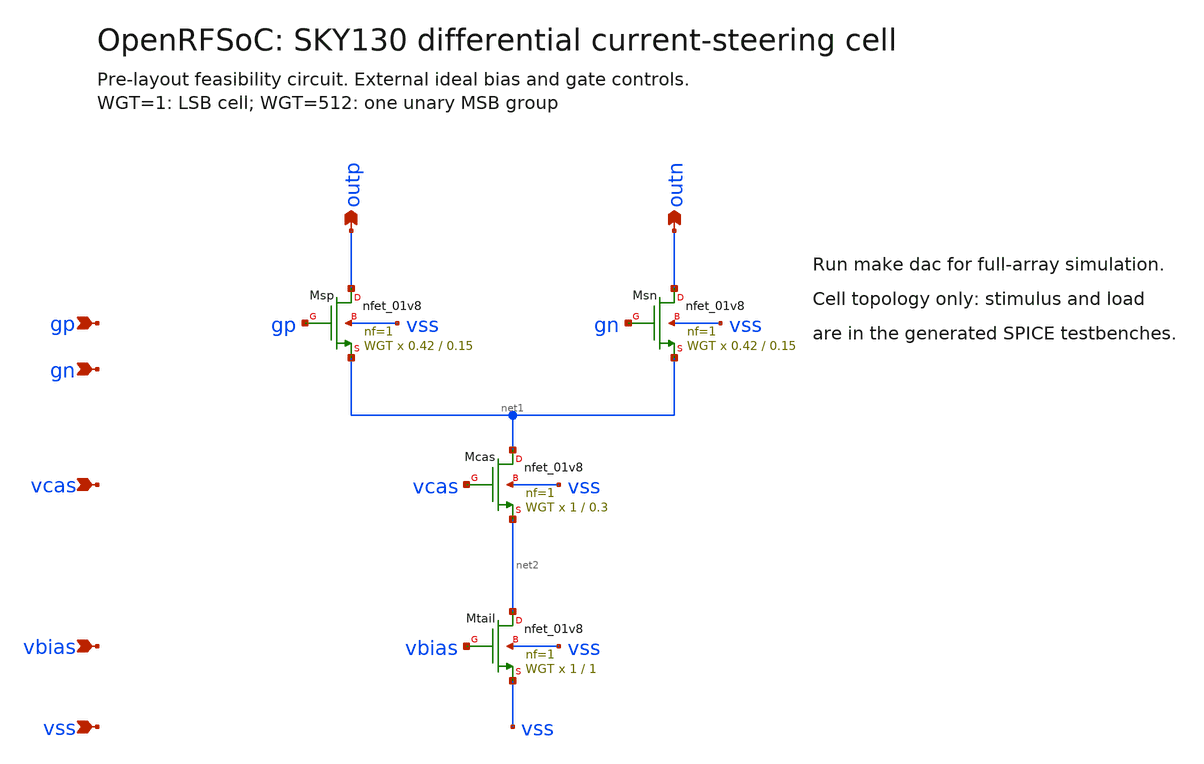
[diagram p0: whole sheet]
** sch_path: analog/dac14_2g/current_cell.sch
**.subckt current_cell outp outn gp gn vcas vbias vss
*.opin outp
*.opin outn
*.ipin gp
*.ipin gn
*.ipin vcas
*.ipin vbias
*.ipin vss
XMsp outp gp net1 vss sky130_fd_pr__nfet_01v8 L=0.15 W=0.42 nf=1 ad='int((1 + 1)/2) * 0.42 / 1 * 0.29'
+ as='int((1 + 2)/2) * 0.42 / 1 * 0.29' pd='2*int((1 + 1)/2) * (0.42 / 1 + 0.29)' ps='2*int((1 + 2)/2) * (0.42 / 1 + 0.29)'
+ nrd=0.333333333333333 nrs=0.333333333333333 sa=0 sb=0 sd=0 mult=WGT m=WGT
XMsn outn gn net1 vss sky130_fd_pr__nfet_01v8 L=0.15 W=0.42 nf=1 ad='int((1 + 1)/2) * 0.42 / 1 * 0.29'
+ as='int((1 + 2)/2) * 0.42 / 1 * 0.29' pd='2*int((1 + 1)/2) * (0.42 / 1 + 0.29)' ps='2*int((1 + 2)/2) * (0.42 / 1 + 0.29)'
+ nrd=0.333333333333333 nrs=0.333333333333333 sa=0 sb=0 sd=0 mult=WGT m=WGT
XMcas net1 vcas net2 vss sky130_fd_pr__nfet_01v8 L=0.3 W=1 nf=1 ad='int((1 + 1)/2) * 1 / 1 * 0.29' as='int((1 + 2)/2) * 1 / 1 * 0.29'
+ pd='2*int((1 + 1)/2) * (1 / 1 + 0.29)' ps='2*int((1 + 2)/2) * (1 / 1 + 0.29)' nrd=0.14 nrs=0.14 sa=0
+ sb=0 sd=0 mult=WGT m=WGT
XMtail net2 vbias vss vss sky130_fd_pr__nfet_01v8 L=1 W=1 nf=1 ad='int((1 + 1)/2) * 1 / 1 * 0.29' as='int((1 + 2)/2) * 1 / 1 * 0.29'
+ pd='2*int((1 + 1)/2) * (1 / 1 + 0.29)' ps='2*int((1 + 2)/2) * (1 / 1 + 0.29)' nrd=0.14 nrs=0.14 sa=0
+ sb=0 sd=0 mult=WGT m=WGT
**** begin user architecture code

.param WGT=1

**** end user architecture code
**.ends
.end
